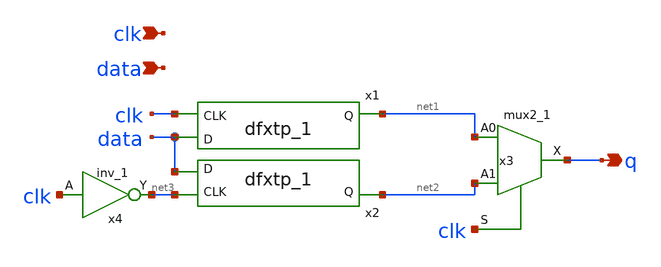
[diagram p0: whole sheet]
** sch_path: xschem/tryandtest/deff.sch
**.subckt deff clk data q
*.ipin clk
*.ipin data
*.opin q
x1 clk data GND GND VDD VDD net1 sky130_fd_sc_lp__dfxtp_1
x2 net3 data GND GND VDD VDD net2 sky130_fd_sc_lp__dfxtp_1
x3 net1 net2 clk GND GND VDD VDD q sky130_fd_sc_lp__mux2_1
x4 clk GND GND VDD VDD net3 sky130_fd_sc_lp__inv_1
**.ends
.end
